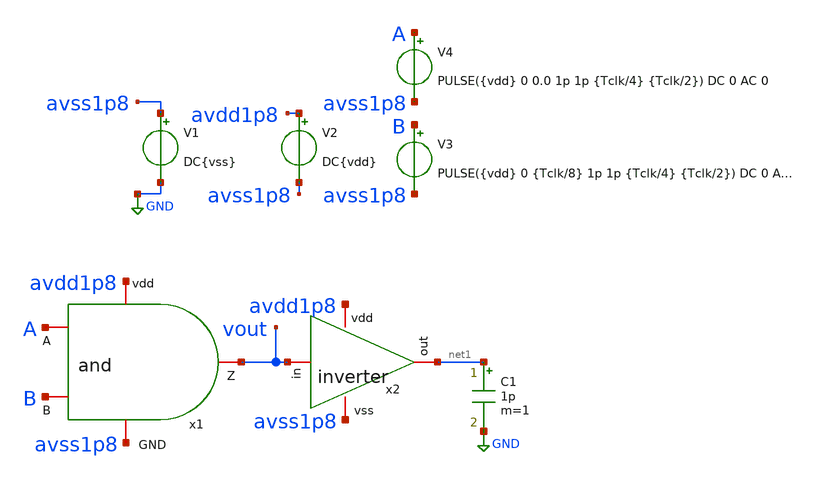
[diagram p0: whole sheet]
** sch_path: simbolos y esquematicos/tb_and.sch
**.subckt tb_and
V3 B avss1p8 PULSE({vdd} 0 {Tclk/8} 1p 1p {Tclk/4} {Tclk/2}) DC 0 AC 0
V1 avss1p8 GND DC{vss}
V2 avdd1p8 avss1p8 DC{vdd}
x2 avdd1p8 vout net1 avss1p8 inverter
C1 net1 GND 1p m=1
V4 A avss1p8 PULSE({vdd} 0 0.0 1p 1p {Tclk/4} {Tclk/2}) DC 0 AC 0
x1 avdd1p8 A vout B avss1p8 and
**** begin user architecture code


* Circuit Parameters
.param vdd= 1.8
.param vss= 0.0
.param Tclk = 50n
.options TEMP = 65.0
* Include Models
.lib /foss/pdks/sky130A/libs.tech/ngspice/sky130.lib.spice TT
* OP Parameters & Singals to save
.save all
*Simulations
.control
tran 0.01u 100n
setplot tran1
plot v(A) v(B)+2 v(vout)+4
reset
dc V3 0 1.8 0.01
setplot dc
plot vin vout ylabel vout xlabel vin
set filetype = ascii
write dcsweep.raw
.endc
.end


**** end user architecture code
**.ends
.GLOBAL GND
.end
